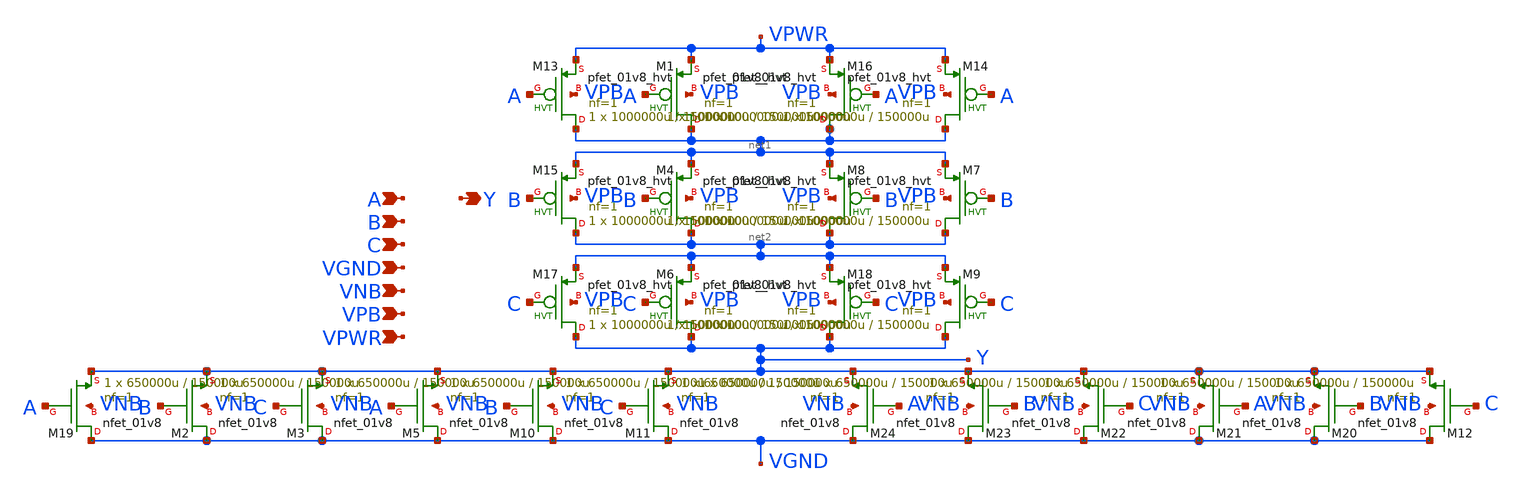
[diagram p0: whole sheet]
** sch_path: schematics/nor3/sky130_fd_sc_hd__nor3_4.sch
**.subckt sky130_fd_sc_hd__nor3_4 A B VGND VNB VPB VPWR Y C
*.ipin A
*.ipin B
*.ipin VGND
*.ipin VNB
*.ipin VPB
*.ipin VPWR
*.opin Y
*.ipin C
XM1 net1 A VPWR VPB sky130_fd_pr__pfet_01v8_hvt L=150000u W=1000000u nf=1 ad='int((1 + 1)/2) * 1000000u / 1 * 0.29'
+ as='int((1 + 2)/2) * 1000000u / 1 * 0.29' pd='2*int((1 + 1)/2) * (1000000u / 1 + 0.29)' ps='2*int((1 + 2)/2) * (1000000u / 1 + 0.29)'
+ nrd='0.29 / 1000000u ' nrs='0.29 / 1000000u ' sa=0 sb=0 sd=0 mult=1 m=1
XM4 net2 B net1 VPB sky130_fd_pr__pfet_01v8_hvt L=150000u W=1000000u nf=1 ad='int((1 + 1)/2) * 1000000u / 1 * 0.29'
+ as='int((1 + 2)/2) * 1000000u / 1 * 0.29' pd='2*int((1 + 1)/2) * (1000000u / 1 + 0.29)' ps='2*int((1 + 2)/2) * (1000000u / 1 + 0.29)'
+ nrd='0.29 / 1000000u ' nrs='0.29 / 1000000u ' sa=0 sb=0 sd=0 mult=1 m=1
XM6 Y C net2 VPB sky130_fd_pr__pfet_01v8_hvt L=150000u W=1000000u nf=1 ad='int((1 + 1)/2) * 1000000u / 1 * 0.29'
+ as='int((1 + 2)/2) * 1000000u / 1 * 0.29' pd='2*int((1 + 1)/2) * (1000000u / 1 + 0.29)' ps='2*int((1 + 2)/2) * (1000000u / 1 + 0.29)'
+ nrd='0.29 / 1000000u ' nrs='0.29 / 1000000u ' sa=0 sb=0 sd=0 mult=1 m=1
XM13 net1 A VPWR VPB sky130_fd_pr__pfet_01v8_hvt L=150000u W=1000000u nf=1 ad='int((1 + 1)/2) * 1000000u / 1 * 0.29'
+ as='int((1 + 2)/2) * 1000000u / 1 * 0.29' pd='2*int((1 + 1)/2) * (1000000u / 1 + 0.29)' ps='2*int((1 + 2)/2) * (1000000u / 1 + 0.29)'
+ nrd='0.29 / 1000000u ' nrs='0.29 / 1000000u ' sa=0 sb=0 sd=0 mult=1 m=1
XM15 net2 B net1 VPB sky130_fd_pr__pfet_01v8_hvt L=150000u W=1000000u nf=1 ad='int((1 + 1)/2) * 1000000u / 1 * 0.29'
+ as='int((1 + 2)/2) * 1000000u / 1 * 0.29' pd='2*int((1 + 1)/2) * (1000000u / 1 + 0.29)' ps='2*int((1 + 2)/2) * (1000000u / 1 + 0.29)'
+ nrd='0.29 / 1000000u ' nrs='0.29 / 1000000u ' sa=0 sb=0 sd=0 mult=1 m=1
XM17 Y C net2 VPB sky130_fd_pr__pfet_01v8_hvt L=150000u W=1000000u nf=1 ad='int((1 + 1)/2) * 1000000u / 1 * 0.29'
+ as='int((1 + 2)/2) * 1000000u / 1 * 0.29' pd='2*int((1 + 1)/2) * (1000000u / 1 + 0.29)' ps='2*int((1 + 2)/2) * (1000000u / 1 + 0.29)'
+ nrd='0.29 / 1000000u ' nrs='0.29 / 1000000u ' sa=0 sb=0 sd=0 mult=1 m=1
XM19 VGND A Y VNB sky130_fd_pr__nfet_01v8 L=150000u W=650000u nf=1 ad='int((1 + 1)/2) * 650000u / 1 * 0.29'
+ as='int((1 + 2)/2) * 650000u / 1 * 0.29' pd='2*int((1 + 1)/2) * (650000u / 1 + 0.29)' ps='2*int((1 + 2)/2) * (650000u / 1 + 0.29)'
+ nrd='0.29 / 650000u ' nrs='0.29 / 650000u ' sa=0 sb=0 sd=0 mult=1 m=1
XM2 VGND B Y VNB sky130_fd_pr__nfet_01v8 L=150000u W=650000u nf=1 ad='int((1 + 1)/2) * 650000u / 1 * 0.29'
+ as='int((1 + 2)/2) * 650000u / 1 * 0.29' pd='2*int((1 + 1)/2) * (650000u / 1 + 0.29)' ps='2*int((1 + 2)/2) * (650000u / 1 + 0.29)'
+ nrd='0.29 / 650000u ' nrs='0.29 / 650000u ' sa=0 sb=0 sd=0 mult=1 m=1
XM3 VGND C Y VNB sky130_fd_pr__nfet_01v8 L=150000u W=650000u nf=1 ad='int((1 + 1)/2) * 650000u / 1 * 0.29'
+ as='int((1 + 2)/2) * 650000u / 1 * 0.29' pd='2*int((1 + 1)/2) * (650000u / 1 + 0.29)' ps='2*int((1 + 2)/2) * (650000u / 1 + 0.29)'
+ nrd='0.29 / 650000u ' nrs='0.29 / 650000u ' sa=0 sb=0 sd=0 mult=1 m=1
XM5 VGND A Y VNB sky130_fd_pr__nfet_01v8 L=150000u W=650000u nf=1 ad='int((1 + 1)/2) * 650000u / 1 * 0.29'
+ as='int((1 + 2)/2) * 650000u / 1 * 0.29' pd='2*int((1 + 1)/2) * (650000u / 1 + 0.29)' ps='2*int((1 + 2)/2) * (650000u / 1 + 0.29)'
+ nrd='0.29 / 650000u ' nrs='0.29 / 650000u ' sa=0 sb=0 sd=0 mult=1 m=1
XM10 VGND B Y VNB sky130_fd_pr__nfet_01v8 L=150000u W=650000u nf=1 ad='int((1 + 1)/2) * 650000u / 1 * 0.29'
+ as='int((1 + 2)/2) * 650000u / 1 * 0.29' pd='2*int((1 + 1)/2) * (650000u / 1 + 0.29)' ps='2*int((1 + 2)/2) * (650000u / 1 + 0.29)'
+ nrd='0.29 / 650000u ' nrs='0.29 / 650000u ' sa=0 sb=0 sd=0 mult=1 m=1
XM11 VGND C Y VNB sky130_fd_pr__nfet_01v8 L=150000u W=650000u nf=1 ad='int((1 + 1)/2) * 650000u / 1 * 0.29'
+ as='int((1 + 2)/2) * 650000u / 1 * 0.29' pd='2*int((1 + 1)/2) * (650000u / 1 + 0.29)' ps='2*int((1 + 2)/2) * (650000u / 1 + 0.29)'
+ nrd='0.29 / 650000u ' nrs='0.29 / 650000u ' sa=0 sb=0 sd=0 mult=1 m=1
XM12 VGND C Y VNB sky130_fd_pr__nfet_01v8 L=150000u W=650000u nf=1 ad='int((1 + 1)/2) * 650000u / 1 * 0.29'
+ as='int((1 + 2)/2) * 650000u / 1 * 0.29' pd='2*int((1 + 1)/2) * (650000u / 1 + 0.29)' ps='2*int((1 + 2)/2) * (650000u / 1 + 0.29)'
+ nrd='0.29 / 650000u ' nrs='0.29 / 650000u ' sa=0 sb=0 sd=0 mult=1 m=1
XM20 VGND B Y VNB sky130_fd_pr__nfet_01v8 L=150000u W=650000u nf=1 ad='int((1 + 1)/2) * 650000u / 1 * 0.29'
+ as='int((1 + 2)/2) * 650000u / 1 * 0.29' pd='2*int((1 + 1)/2) * (650000u / 1 + 0.29)' ps='2*int((1 + 2)/2) * (650000u / 1 + 0.29)'
+ nrd='0.29 / 650000u ' nrs='0.29 / 650000u ' sa=0 sb=0 sd=0 mult=1 m=1
XM21 VGND A Y VNB sky130_fd_pr__nfet_01v8 L=150000u W=650000u nf=1 ad='int((1 + 1)/2) * 650000u / 1 * 0.29'
+ as='int((1 + 2)/2) * 650000u / 1 * 0.29' pd='2*int((1 + 1)/2) * (650000u / 1 + 0.29)' ps='2*int((1 + 2)/2) * (650000u / 1 + 0.29)'
+ nrd='0.29 / 650000u ' nrs='0.29 / 650000u ' sa=0 sb=0 sd=0 mult=1 m=1
XM22 VGND C Y VNB sky130_fd_pr__nfet_01v8 L=150000u W=650000u nf=1 ad='int((1 + 1)/2) * 650000u / 1 * 0.29'
+ as='int((1 + 2)/2) * 650000u / 1 * 0.29' pd='2*int((1 + 1)/2) * (650000u / 1 + 0.29)' ps='2*int((1 + 2)/2) * (650000u / 1 + 0.29)'
+ nrd='0.29 / 650000u ' nrs='0.29 / 650000u ' sa=0 sb=0 sd=0 mult=1 m=1
XM23 VGND B Y VNB sky130_fd_pr__nfet_01v8 L=150000u W=650000u nf=1 ad='int((1 + 1)/2) * 650000u / 1 * 0.29'
+ as='int((1 + 2)/2) * 650000u / 1 * 0.29' pd='2*int((1 + 1)/2) * (650000u / 1 + 0.29)' ps='2*int((1 + 2)/2) * (650000u / 1 + 0.29)'
+ nrd='0.29 / 650000u ' nrs='0.29 / 650000u ' sa=0 sb=0 sd=0 mult=1 m=1
XM24 VGND A Y VNB sky130_fd_pr__nfet_01v8 L=150000u W=650000u nf=1 ad='int((1 + 1)/2) * 650000u / 1 * 0.29'
+ as='int((1 + 2)/2) * 650000u / 1 * 0.29' pd='2*int((1 + 1)/2) * (650000u / 1 + 0.29)' ps='2*int((1 + 2)/2) * (650000u / 1 + 0.29)'
+ nrd='0.29 / 650000u ' nrs='0.29 / 650000u ' sa=0 sb=0 sd=0 mult=1 m=1
XM9 Y C net2 VPB sky130_fd_pr__pfet_01v8_hvt L=150000u W=1000000u nf=1 ad='int((1 + 1)/2) * 1000000u / 1 * 0.29'
+ as='int((1 + 2)/2) * 1000000u / 1 * 0.29' pd='2*int((1 + 1)/2) * (1000000u / 1 + 0.29)' ps='2*int((1 + 2)/2) * (1000000u / 1 + 0.29)'
+ nrd='0.29 / 1000000u ' nrs='0.29 / 1000000u ' sa=0 sb=0 sd=0 mult=1 m=1
XM18 Y C net2 VPB sky130_fd_pr__pfet_01v8_hvt L=150000u W=1000000u nf=1 ad='int((1 + 1)/2) * 1000000u / 1 * 0.29'
+ as='int((1 + 2)/2) * 1000000u / 1 * 0.29' pd='2*int((1 + 1)/2) * (1000000u / 1 + 0.29)' ps='2*int((1 + 2)/2) * (1000000u / 1 + 0.29)'
+ nrd='0.29 / 1000000u ' nrs='0.29 / 1000000u ' sa=0 sb=0 sd=0 mult=1 m=1
XM7 net2 B net1 VPB sky130_fd_pr__pfet_01v8_hvt L=150000u W=1000000u nf=1 ad='int((1 + 1)/2) * 1000000u / 1 * 0.29'
+ as='int((1 + 2)/2) * 1000000u / 1 * 0.29' pd='2*int((1 + 1)/2) * (1000000u / 1 + 0.29)' ps='2*int((1 + 2)/2) * (1000000u / 1 + 0.29)'
+ nrd='0.29 / 1000000u ' nrs='0.29 / 1000000u ' sa=0 sb=0 sd=0 mult=1 m=1
XM8 net2 B net1 VPB sky130_fd_pr__pfet_01v8_hvt L=150000u W=1000000u nf=1 ad='int((1 + 1)/2) * 1000000u / 1 * 0.29'
+ as='int((1 + 2)/2) * 1000000u / 1 * 0.29' pd='2*int((1 + 1)/2) * (1000000u / 1 + 0.29)' ps='2*int((1 + 2)/2) * (1000000u / 1 + 0.29)'
+ nrd='0.29 / 1000000u ' nrs='0.29 / 1000000u ' sa=0 sb=0 sd=0 mult=1 m=1
XM14 net1 A VPWR VPB sky130_fd_pr__pfet_01v8_hvt L=150000u W=1000000u nf=1 ad='int((1 + 1)/2) * 1000000u / 1 * 0.29'
+ as='int((1 + 2)/2) * 1000000u / 1 * 0.29' pd='2*int((1 + 1)/2) * (1000000u / 1 + 0.29)' ps='2*int((1 + 2)/2) * (1000000u / 1 + 0.29)'
+ nrd='0.29 / 1000000u ' nrs='0.29 / 1000000u ' sa=0 sb=0 sd=0 mult=1 m=1
XM16 net1 A VPWR VPB sky130_fd_pr__pfet_01v8_hvt L=150000u W=1000000u nf=1 ad='int((1 + 1)/2) * 1000000u / 1 * 0.29'
+ as='int((1 + 2)/2) * 1000000u / 1 * 0.29' pd='2*int((1 + 1)/2) * (1000000u / 1 + 0.29)' ps='2*int((1 + 2)/2) * (1000000u / 1 + 0.29)'
+ nrd='0.29 / 1000000u ' nrs='0.29 / 1000000u ' sa=0 sb=0 sd=0 mult=1 m=1
**.ends
.end
